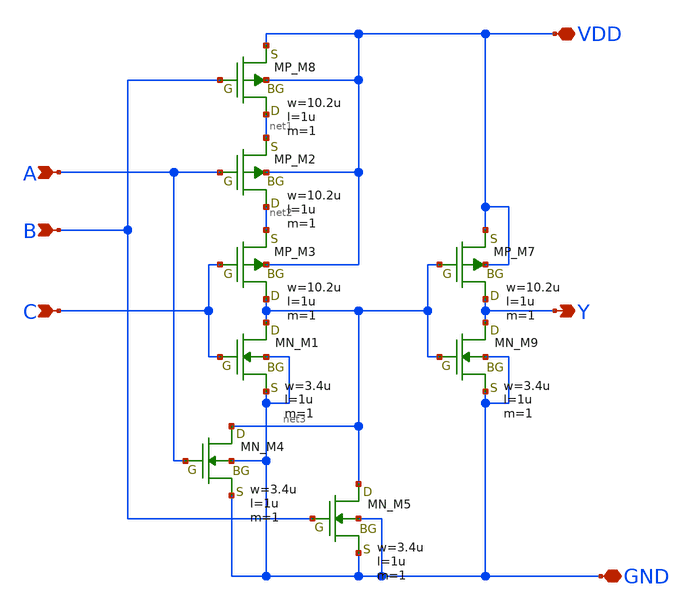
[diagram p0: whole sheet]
** sch_path: libs.tech/xschem/TR-1um_5_stdcell/OR3.sch
**.subckt OR3 A B Y VDD GND C
*.ipin A
*.ipin B
*.opin Y
*.iopin VDD
*.iopin GND
*.ipin C
XM8 net1 B VDD VDD PMOS w=10.2u l=1u nrd=0 nrs=0 m=1
XM2 net2 A net1 VDD PMOS w=10.2u l=1u nrd=0 nrs=0 m=1
XM3 net3 C net2 VDD PMOS w=10.2u l=1u nrd=0 nrs=0 m=1
XM7 Y net3 VDD VDD PMOS w=10.2u l=1u nrd=0 nrs=0 m=1
XM9 Y net3 GND GND NMOS w=3.4u l=1u nrd=0 nrs=0 m=1
XM1 net3 C GND GND NMOS w=3.4u l=1u nrd=0 nrs=0 m=1
XM4 net3 A GND GND NMOS w=3.4u l=1u nrd=0 nrs=0 m=1
XM5 net3 B GND GND NMOS w=3.4u l=1u nrd=0 nrs=0 m=1
**.ends
.end
